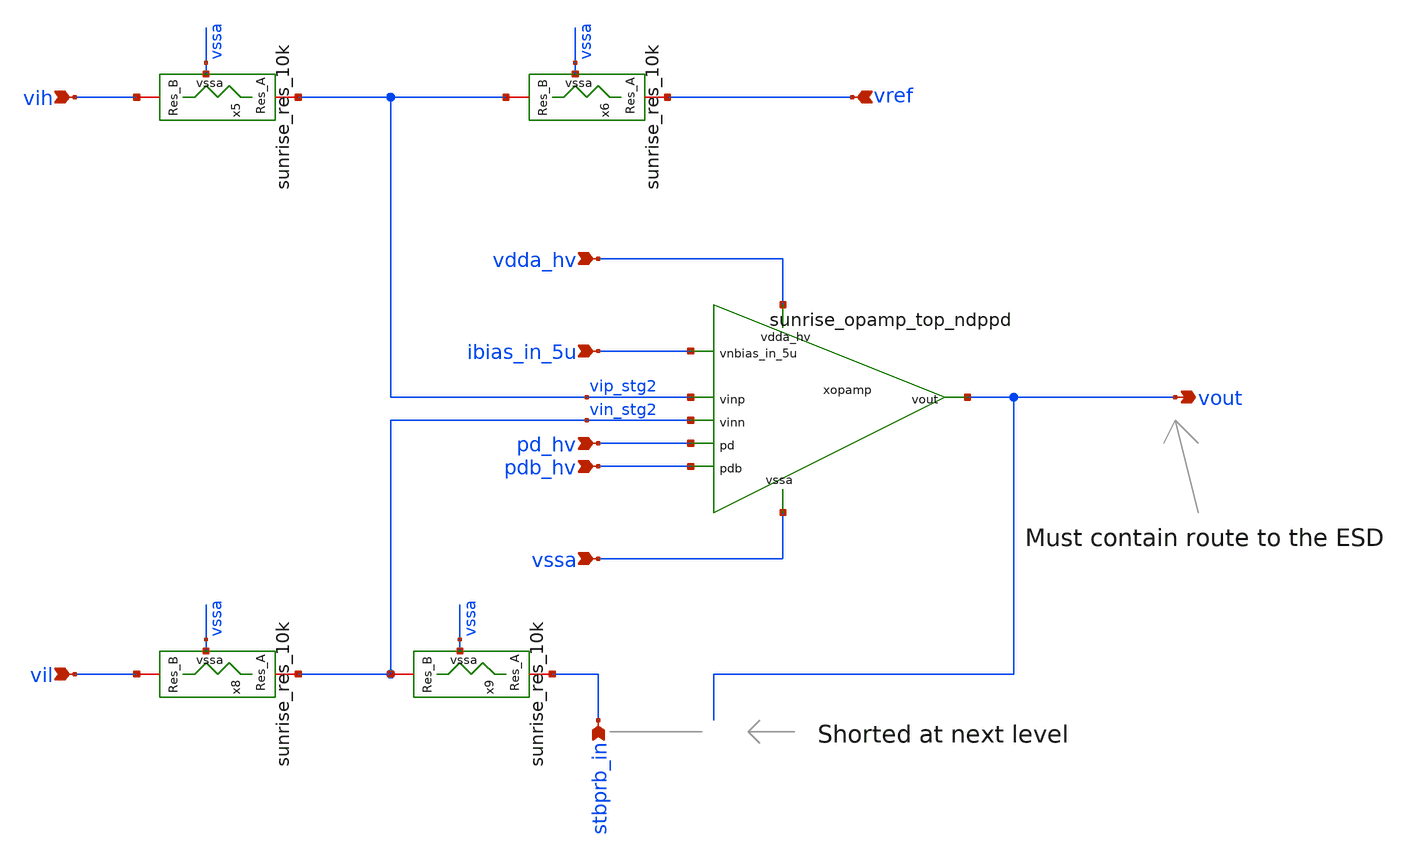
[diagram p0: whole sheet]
** sch_path: Schematics_Layout/sunrise_STG2_loop/sunrise_STG2_loop.sch
**.subckt sunrise_STG2_loop pd_hv pdb_hv ibias_in_5u vdda_hv vssa vil vih vout vref stbprb_in
*.ipin pd_hv
*.ipin pdb_hv
*.ipin ibias_in_5u
*.ipin vdda_hv
*.ipin vssa
*.ipin vil
*.ipin vih
*.opin vout
*.ipin vref
*.ipin stbprb_in
x5 vssa vih vip_stg2 sunrise_res_10k
x6 vssa vip_stg2 vref sunrise_res_10k
x8 vssa vil vin_stg2 sunrise_res_10k
x9 vssa vin_stg2 stbprb_in sunrise_res_10k
xopamp vdda_hv ibias_in_5u vout vip_stg2 vin_stg2 pd_hv pdb_hv vssa sunrise_opamp_top_ndppd
**.ends
.end
